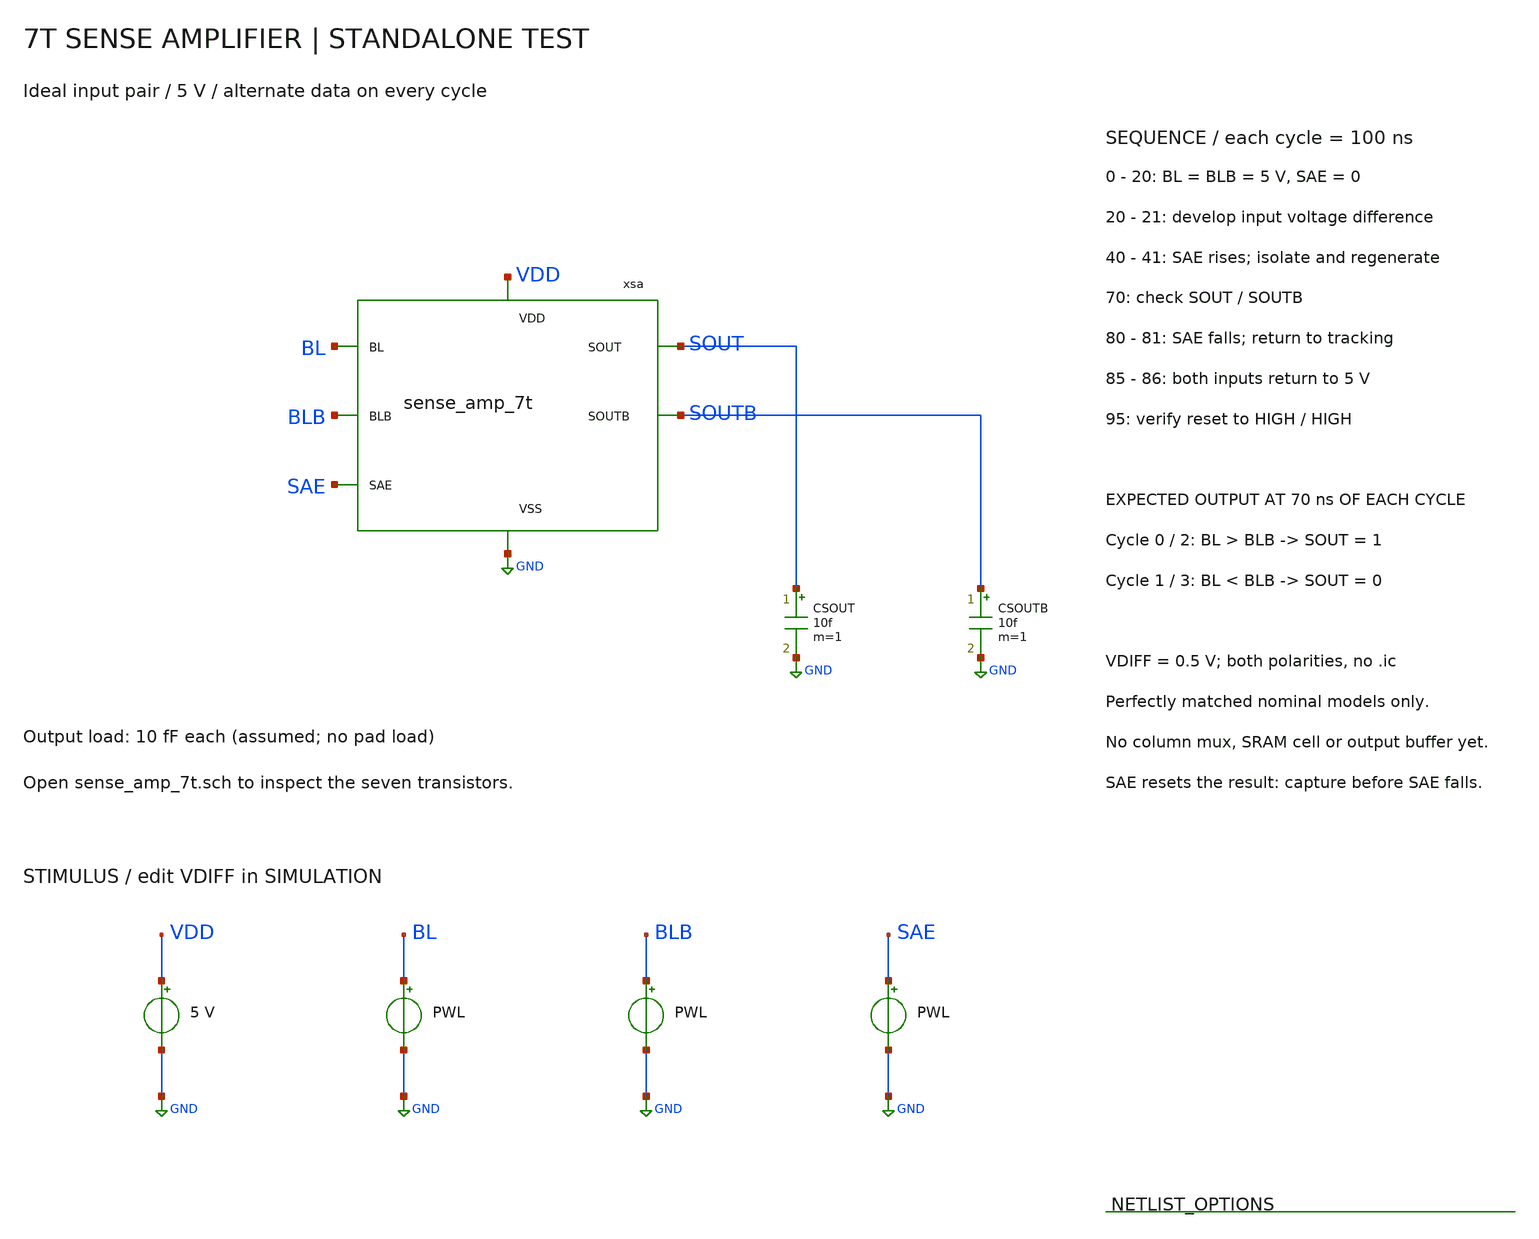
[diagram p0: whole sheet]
** sch_path: member_project/SRAM/PenguinEino/learning/schematics/sram_tb_sense_amp.sch
**.subckt sram_tb_sense_amp
xsa BL BLB SAE SOUT SOUTB VDD GND sense_amp_7t
CSOUT SOUT GND 10f m=1
CSOUTB SOUTB GND 10f m=1
VVDD VDD GND 5
VBL BL GND PWL(0n 5 120n 5 121n '5-VDIFF' 185n '5-VDIFF' 186n 5 320n 5 321n '5-VDIFF' 385n '5-VDIFF'
+ 386n 5 400n 5)
VBLB BLB GND PWL(0n 5 20n 5 21n '5-VDIFF' 85n '5-VDIFF' 86n 5 220n 5 221n '5-VDIFF' 285n '5-VDIFF' 286n
+ 5 400n 5)
VSAE SAE GND PWL(0n 0 40n 0 41n 5 80n 5 81n 0 140n 0 141n 5 180n 5 181n 0 240n 0 241n 5 280n 5 281n
+ 0 340n 0 341n 5 380n 5 381n 0 400n 0)
**** begin user architecture code
 .include $::LIB/ip62_models

.param VDIFF=0.5
.control
save all
tran 0.02n 400n
let failures = 0
meas tran out_0 find v(SOUT) at=70n
meas tran outb_0 find v(SOUTB) at=70n
if out_0 < 4.5 or outb_0 > 0.5
 let failures = failures + 1
end
meas tran reset_0 find v(SOUT) at=95n
meas tran resetb_0 find v(SOUTB) at=95n
if reset_0 < 4.5 or resetb_0 < 4.5
 let failures = failures + 1
end
meas tran out_1 find v(SOUT) at=170n
meas tran outb_1 find v(SOUTB) at=170n
if out_1 > 0.5 or outb_1 < 4.5
 let failures = failures + 1
end
meas tran reset_1 find v(SOUT) at=195n
meas tran resetb_1 find v(SOUTB) at=195n
if reset_1 < 4.5 or resetb_1 < 4.5
 let failures = failures + 1
end
meas tran out_2 find v(SOUT) at=270n
meas tran outb_2 find v(SOUTB) at=270n
if out_2 < 4.5 or outb_2 > 0.5
 let failures = failures + 1
end
meas tran reset_2 find v(SOUT) at=295n
meas tran resetb_2 find v(SOUTB) at=295n
if reset_2 < 4.5 or resetb_2 < 4.5
 let failures = failures + 1
end
meas tran out_3 find v(SOUT) at=370n
meas tran outb_3 find v(SOUTB) at=370n
if out_3 > 0.5 or outb_3 < 4.5
 let failures = failures + 1
end
meas tran reset_3 find v(SOUT) at=395n
meas tran resetb_3 find v(SOUTB) at=395n
if reset_3 < 4.5 or resetb_3 < 4.5
 let failures = failures + 1
end
if failures = 0
 echo PASS: both input polarities, alternating reads and reset
else
 echo FAIL: inspect output and reset measurements
 print failures
end
write sram_tb_sense_amp.raw
plot v(BL) v(BLB) ylimit 4.3 5.2 title 'INPUTS: precharge and differential voltage'
plot v(SOUT) v(SOUTB) ylimit -0.5 5.5 title 'OUTPUTS: valid while SAE is HIGH'
plot v(SAE) ylimit -0.5 5.5 title 'SAE: LOW tracks / HIGH regenerates'
.endc

**** end user architecture code
**.ends

* expanding   symbol:  sense_amp_7t.sym # of pins=7
** sym_path: member_project/SRAM/PenguinEino/sram512/schematics/sense_amp_7t.sym
** sch_path: member_project/SRAM/PenguinEino/sram512/schematics/sense_amp_7t.sch
.subckt sense_amp_7t BL BLB SAE SOUT SOUTB VDD VSS
*.ipin BL
*.ipin BLB
*.opin SOUT
*.opin SOUTB
*.iopin VSS
*.iopin VDD
*.ipin SAE
XXP_ISO_L SOUT SAE BL VDD PMOS w=3.4u l=1u nrd=0 nrs=0 m=1
XXP_ISO_R SOUTB SAE BLB VDD PMOS w=3.4u l=1u nrd=0 nrs=0 m=1
XXP_L SOUT SOUTB VDD VDD PMOS w=3.4u l=1u nrd=0 nrs=0 m=1
XXN_L SOUT SOUTB net1 VSS NMOS w=3.4u l=1u nrd=0 nrs=0 m=1
XXP_R SOUTB SOUT VDD VDD PMOS w=3.4u l=1u nrd=0 nrs=0 m=1
XXN_R SOUTB SOUT net1 VSS NMOS w=3.4u l=1u nrd=0 nrs=0 m=1
XXN_TAIL net1 SAE VSS VSS NMOS w=3.4u l=1u nrd=0 nrs=0 m=1
.ends

.GLOBAL GND
.end
